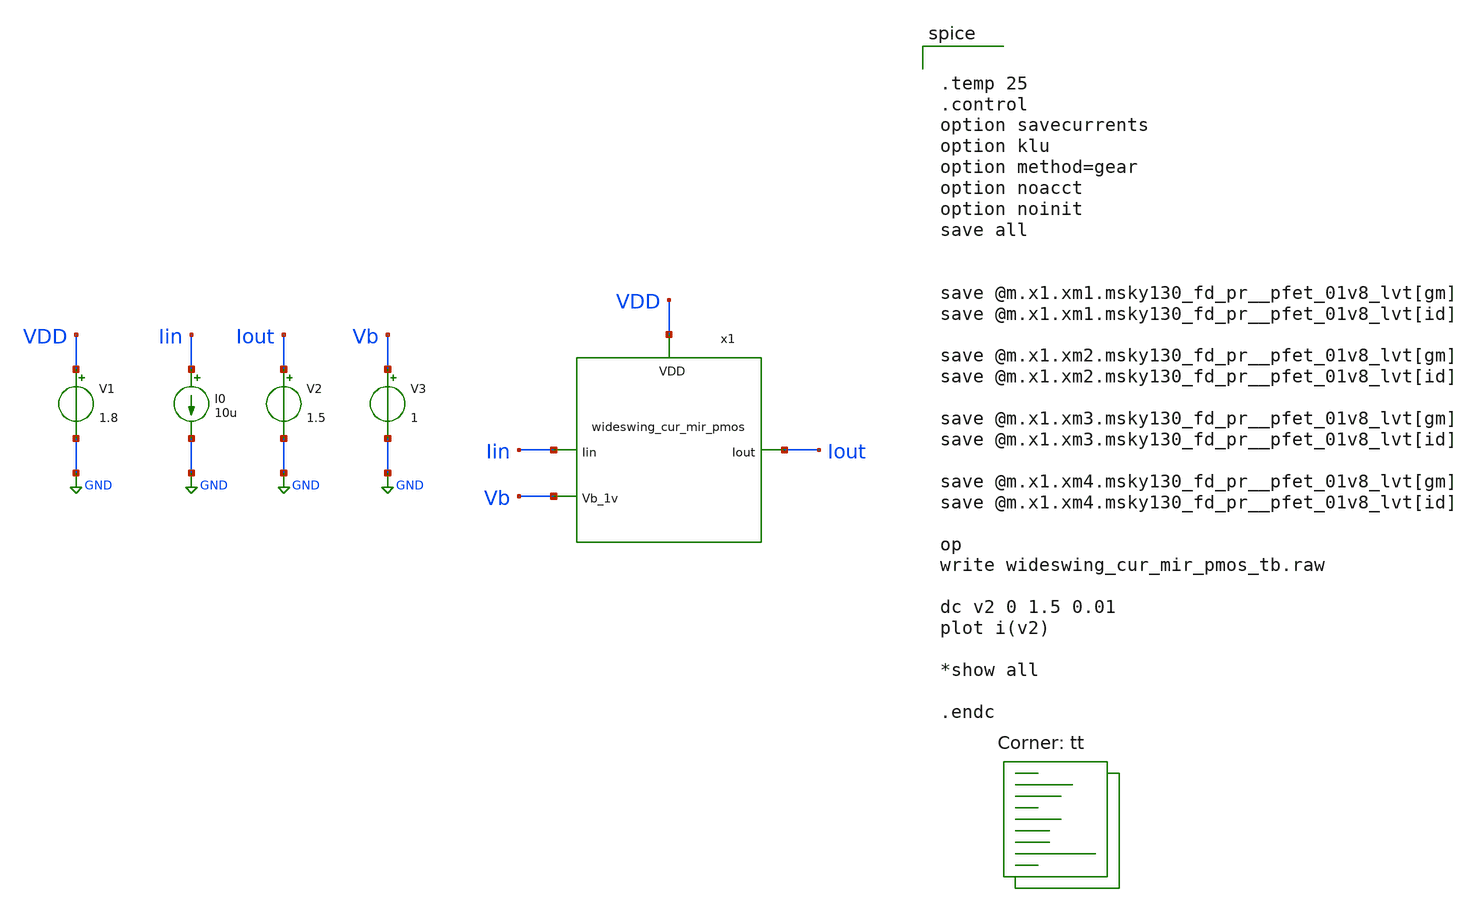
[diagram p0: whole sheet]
** sch_path: xschem/wideswing_cur_mir_pmos_tb.sch
**.subckt wideswing_cur_mir_pmos_tb
V1 VDD GND 1.8
.save i(v1)
I0 Iin GND 10u
V2 Iout GND 1.5
.save i(v2)
V3 Vb GND 1
.save i(v3)
x1 VDD Vb Iin Iout wideswing_cur_mir_pmos
**** begin user architecture code


.temp 25
.control
option savecurrents
option klu
option method=gear
option noacct
option noinit
save all


save @m.x1.xm1.msky130_fd_pr__pfet_01v8_lvt[gm]
save @m.x1.xm1.msky130_fd_pr__pfet_01v8_lvt[id]

save @m.x1.xm2.msky130_fd_pr__pfet_01v8_lvt[gm]
save @m.x1.xm2.msky130_fd_pr__pfet_01v8_lvt[id]

save @m.x1.xm3.msky130_fd_pr__pfet_01v8_lvt[gm]
save @m.x1.xm3.msky130_fd_pr__pfet_01v8_lvt[id]

save @m.x1.xm4.msky130_fd_pr__pfet_01v8_lvt[gm]
save @m.x1.xm4.msky130_fd_pr__pfet_01v8_lvt[id]

op
write wideswing_cur_mir_pmos_tb.raw

dc v2 0 1.5 0.01
plot i(v2)

*show all

.endc

.lib $::SKYWATER_MODELS/sky130.lib.spice tt
**** end user architecture code
**.ends

* expanding   symbol:  wideswing_cur_mir_pmos.sym # of pins=4
** sym_path: xschem/wideswing_cur_mir_pmos.sym
** sch_path: xschem/wideswing_cur_mir_pmos.sch
.subckt wideswing_cur_mir_pmos VDD Vb_1v Iin Iout
*.opin Iout
*.ipin Iin
*.ipin Vb_1v
*.iopin VDD
XM1 net1 Iin VDD VDD sky130_fd_pr__pfet_01v8_lvt L=8 W=200 nf=1 ad='int((1 + 1)/2) * 200 / 1 * 0.29'
+ as='int((1 + 2)/2) * 200 / 1 * 0.29' pd='2*int((1 + 1)/2) * (200 / 1 + 0.29)' ps='2*int((1 + 2)/2) * (200 / 1 + 0.29)'
+ nrd='0.29 / 200 ' nrs='0.29 / 200 ' sa=0 sb=0 sd=0 mult=2 m=2
XM2 Iin Vb_1v net1 VDD sky130_fd_pr__pfet_01v8_lvt L=8 W=200 nf=1 ad='int((1 + 1)/2) * 200 / 1 * 0.29'
+ as='int((1 + 2)/2) * 200 / 1 * 0.29' pd='2*int((1 + 1)/2) * (200 / 1 + 0.29)' ps='2*int((1 + 2)/2) * (200 / 1 + 0.29)'
+ nrd='0.29 / 200 ' nrs='0.29 / 200 ' sa=0 sb=0 sd=0 mult=2 m=2
XM3 net2 Iin VDD VDD sky130_fd_pr__pfet_01v8_lvt L=8 W=200 nf=1 ad='int((1 + 1)/2) * 200 / 1 * 0.29'
+ as='int((1 + 2)/2) * 200 / 1 * 0.29' pd='2*int((1 + 1)/2) * (200 / 1 + 0.29)' ps='2*int((1 + 2)/2) * (200 / 1 + 0.29)'
+ nrd='0.29 / 200 ' nrs='0.29 / 200 ' sa=0 sb=0 sd=0 mult=2 m=2
XM4 Iout Vb_1v net2 VDD sky130_fd_pr__pfet_01v8_lvt L=8 W=200 nf=1 ad='int((1 + 1)/2) * 200 / 1 * 0.29'
+ as='int((1 + 2)/2) * 200 / 1 * 0.29' pd='2*int((1 + 1)/2) * (200 / 1 + 0.29)' ps='2*int((1 + 2)/2) * (200 / 1 + 0.29)'
+ nrd='0.29 / 200 ' nrs='0.29 / 200 ' sa=0 sb=0 sd=0 mult=2 m=2
.ends

.GLOBAL GND
.end
